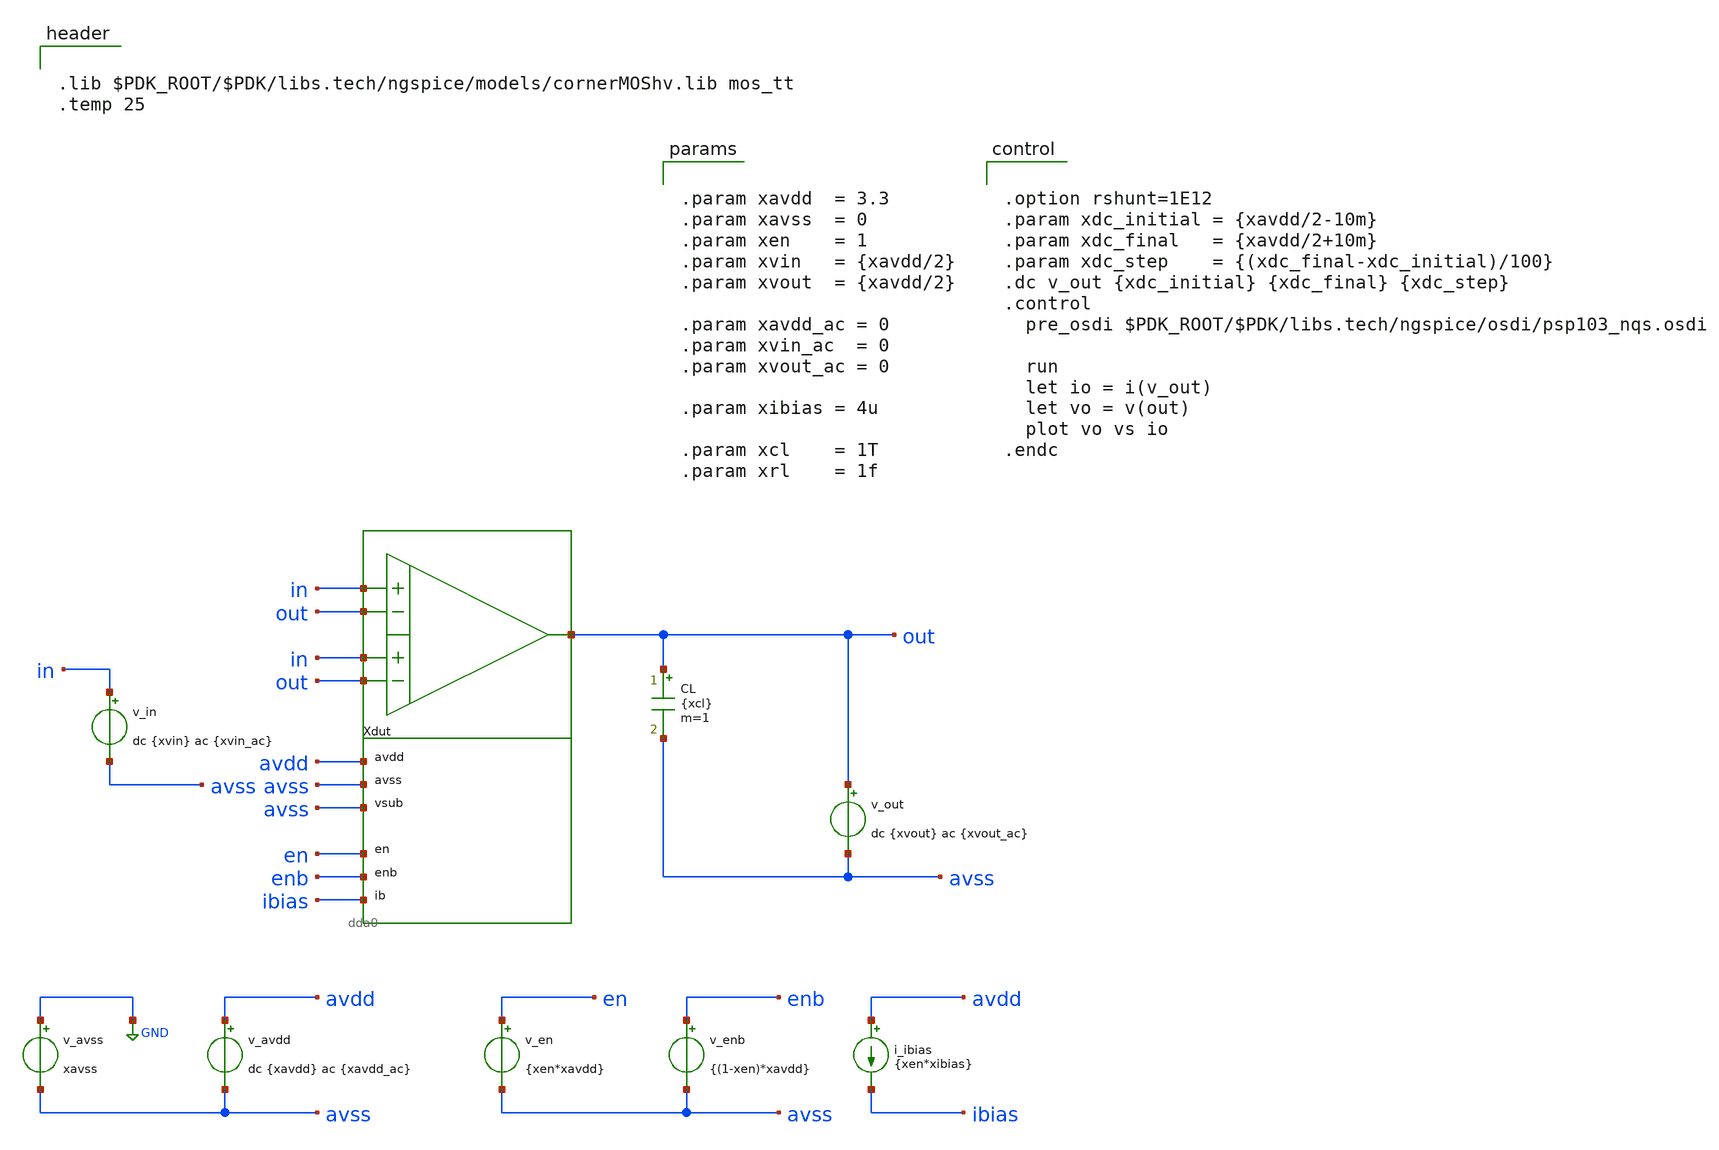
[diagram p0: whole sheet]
** sch_path: xschem/tb_dda0_buf_io.sch
**.subckt tb_dda0_buf_io
Xdut in out in out out avdd avss avss en enb ibias dda0
v_avss GND avss xavss
v_avdd avdd avss dc {xavdd} ac {xavdd_ac}
v_in in avss dc {xvin} ac {xvin_ac}
v_en en avss {xen*xavdd}
v_enb enb avss {(1-xen)*xavdd}
i_ibias avdd ibias {xen*xibias}
CL out avss {xcl} m=1
v_out out avss dc {xvout} ac {xvout_ac}
**** begin user architecture code


.lib $PDK_ROOT/$PDK/libs.tech/ngspice/models/cornerMOShv.lib mos_tt
.temp 25




.option rshunt=1E12
.param xdc_initial = {xavdd/2-10m}
.param xdc_final   = {xavdd/2+10m}
.param xdc_step    = {(xdc_final-xdc_initial)/100}
.dc v_out {xdc_initial} {xdc_final} {xdc_step}
.control
  pre_osdi $PDK_ROOT/$PDK/libs.tech/ngspice/osdi/psp103_nqs.osdi

  run
  let io = i(v_out)
  let vo = v(out)
  plot vo vs io
.endc




.param xavdd  = 3.3
.param xavss  = 0
.param xen    = 1
.param xvin   = {xavdd/2}
.param xvout  = {xavdd/2}

.param xavdd_ac = 0
.param xvin_ac  = 0
.param xvout_ac = 0

.param xibias = 4u

.param xcl    = 1T
.param xrl    = 1f


**** end user architecture code
**.ends
.GLOBAL GND
.end
